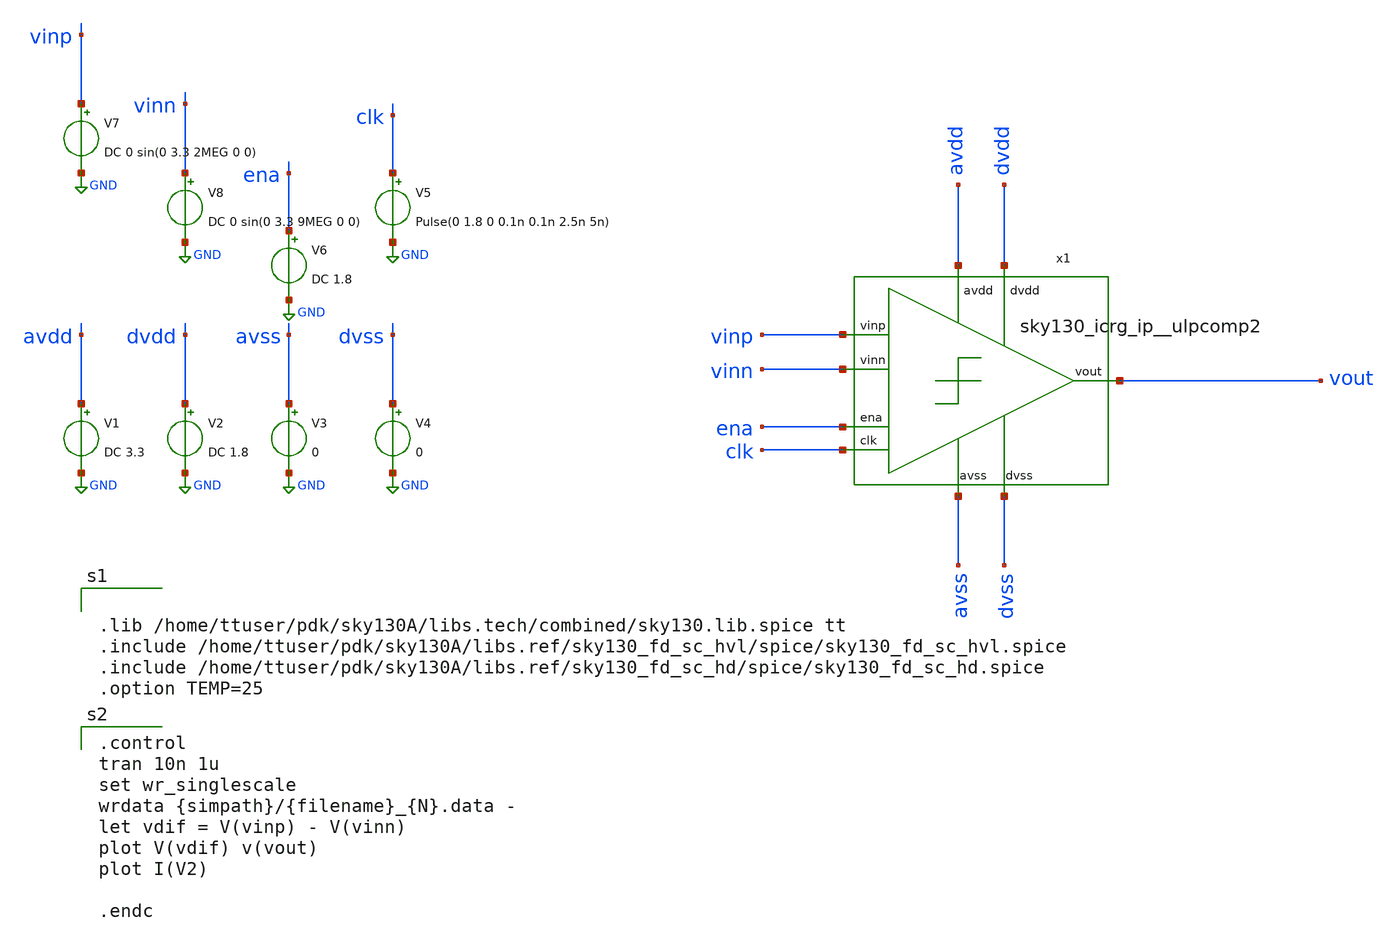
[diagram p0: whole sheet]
** sch_path: xschem/dynamic_current_tb.sch
**.subckt dynamic_current_tb
x1 dvdd avdd ena vout vinn vinp clk dvss avss sky130_icrg_ip__ulpcomp2
V1 avdd GND DC 3.3
V2 dvdd GND DC 1.8
V3 avss GND 0
V4 dvss GND 0
V5 clk GND Pulse(0 1.8 0 0.1n 0.1n 2.5n 5n)
V6 ena GND DC 1.8
V7 vinp GND DC 0 sin(0 3.3 2MEG 0 0)
V8 vinn GND DC 0 sin(0 3.3 9MEG 0 0)
**** begin user architecture code


.lib /home/ttuser/pdk/sky130A/libs.tech/combined/sky130.lib.spice tt
.include /home/ttuser/pdk/sky130A/libs.ref/sky130_fd_sc_hvl/spice/sky130_fd_sc_hvl.spice
.include /home/ttuser/pdk/sky130A/libs.ref/sky130_fd_sc_hd/spice/sky130_fd_sc_hd.spice
.option TEMP=25


.control
tran 10n 1u
set wr_singlescale
wrdata {simpath}/{filename}_{N}.data -
let vdif = V(vinp) - V(vinn)
plot V(vdif) v(vout)
plot I(V2)

.endc

**** end user architecture code
**.ends

* expanding   symbol:  sky130_icrg_ip__ulpcomp2.sym # of pins=9
** sym_path: xschem/sky130_icrg_ip__ulpcomp2.sym
** sch_path: xschem/sky130_icrg_ip__ulpcomp2.sch
.subckt sky130_icrg_ip__ulpcomp2 dvdd avdd ena vout vinn vinp clk dvss avss
*.ipin avdd
*.ipin vinp
*.ipin vinn
*.opin avss
*.opin vout
*.opin dvss
*.ipin dvdd
*.ipin clk
*.ipin ena
x1 dvddb clka clk clkb dvss Stage0_clk_inv
x2 avdd enab clka vinn vinp net2 net1 avss Stage1
x3 dvdd enab dvddb clkb vout net2 net1 dvss Stage2_latch
x4 dvdd ena enab dvss Stage0_ena_inv
.ends


* expanding   symbol:  Stage0_clk_inv.sym # of pins=5
** sym_path: xschem/Stage0_clk_inv.sym
** sch_path: xschem/Stage0_clk_inv.sch
.subckt Stage0_clk_inv dvddb clka clk clkb dvss
*.opin dvss
*.ipin dvddb
*.opin clka
*.ipin clk
*.opin clkb
XM22 clka clkb dvddb dvddb sky130_fd_pr__pfet_01v8 L=0.5 W=2 nf=1 ad='int((nf+1)/2) * W/nf * 0.29' as='int((nf+2)/2) * W/nf * 0.29'
+ pd='2*int((nf+1)/2) * (W/nf + 0.29)' ps='2*int((nf+2)/2) * (W/nf + 0.29)' nrd='0.29 / W' nrs='0.29 / W'
+ sa=0 sb=0 sd=0 mult=1 m=1
XM8 clkb clk dvddb dvddb sky130_fd_pr__pfet_01v8 L=0.5 W=2 nf=1 ad='int((nf+1)/2) * W/nf * 0.29' as='int((nf+2)/2) * W/nf * 0.29'
+ pd='2*int((nf+1)/2) * (W/nf + 0.29)' ps='2*int((nf+2)/2) * (W/nf + 0.29)' nrd='0.29 / W' nrs='0.29 / W'
+ sa=0 sb=0 sd=0 mult=1 m=1
XM6 clkb clk dvss dvss sky130_fd_pr__nfet_01v8 L=0.5 W=1 nf=1 ad='int((nf+1)/2) * W/nf * 0.29' as='int((nf+2)/2) * W/nf * 0.29'
+ pd='2*int((nf+1)/2) * (W/nf + 0.29)' ps='2*int((nf+2)/2) * (W/nf + 0.29)' nrd='0.29 / W' nrs='0.29 / W'
+ sa=0 sb=0 sd=0 mult=1 m=1
XM21 clka clkb dvss dvss sky130_fd_pr__nfet_01v8 L=0.5 W=1 nf=1 ad='int((nf+1)/2) * W/nf * 0.29' as='int((nf+2)/2) * W/nf * 0.29'
+ pd='2*int((nf+1)/2) * (W/nf + 0.29)' ps='2*int((nf+2)/2) * (W/nf + 0.29)' nrd='0.29 / W' nrs='0.29 / W'
+ sa=0 sb=0 sd=0 mult=1 m=1
.ends


* expanding   symbol:  Stage1.sym # of pins=8
** sym_path: xschem/Stage1.sym
** sch_path: xschem/Stage1.sch
.subckt Stage1 avdd enab clka vinn vinp oneg opos avss
*.ipin avdd
*.ipin vinp
*.ipin vinn
*.opin avss
*.opin opos
*.opin oneg
*.ipin clka
*.ipin enab
XM1 net4 net5 avdd avdd sky130_fd_pr__pfet_g5v0d10v5 L=1 W=50 nf=2 ad='int((nf+1)/2) * W/nf * 0.29' as='int((nf+2)/2) * W/nf * 0.29'
+ pd='2*int((nf+1)/2) * (W/nf + 0.29)' ps='2*int((nf+2)/2) * (W/nf + 0.29)' nrd='0.29 / W' nrs='0.29 / W'
+ sa=0 sb=0 sd=0 mult=2 m=2
x2 clka dvdd dvss dvss avdd avdd net2 sky130_fd_sc_hvl__lsbuflv2hv_1
XM6 net1 net2 net4 net4 sky130_fd_pr__pfet_g5v0d10v5 L=1 W=50 nf=2 ad='int((nf+1)/2) * W/nf * 0.29' as='int((nf+2)/2) * W/nf * 0.29'
+ pd='2*int((nf+1)/2) * (W/nf + 0.29)' ps='2*int((nf+2)/2) * (W/nf + 0.29)' nrd='0.29 / W' nrs='0.29 / W'
+ sa=0 sb=0 sd=0 mult=2 m=2
XM2 oneg vinp net1 net1 sky130_fd_pr__pfet_g5v0d10v5 L=1 W=20 nf=2 ad='int((nf+1)/2) * W/nf * 0.29' as='int((nf+2)/2) * W/nf * 0.29'
+ pd='2*int((nf+1)/2) * (W/nf + 0.29)' ps='2*int((nf+2)/2) * (W/nf + 0.29)' nrd='0.29 / W' nrs='0.29 / W'
+ sa=0 sb=0 sd=0 mult=2 m=2
XM3 opos vinn net1 net1 sky130_fd_pr__pfet_g5v0d10v5 L=1 W=20 nf=2 ad='int((nf+1)/2) * W/nf * 0.29' as='int((nf+2)/2) * W/nf * 0.29'
+ pd='2*int((nf+1)/2) * (W/nf + 0.29)' ps='2*int((nf+2)/2) * (W/nf + 0.29)' nrd='0.29 / W' nrs='0.29 / W'
+ sa=0 sb=0 sd=0 mult=2 m=2
XM4 net3 net3 avss avss sky130_fd_pr__nfet_03v3_nvt L=0.5 W=5 nf=1 ad='int((nf+1)/2) * W/nf * 0.29' as='int((nf+2)/2) * W/nf * 0.29'
+ pd='2*int((nf+1)/2) * (W/nf + 0.29)' ps='2*int((nf+2)/2) * (W/nf + 0.29)' nrd='0.29 / W' nrs='0.29 / W'
+ sa=0 sb=0 sd=0 mult=2 m=2
XM8 opos net2 net3 net3 sky130_fd_pr__nfet_g5v0d10v5 L=0.5 W=5 nf=1 ad='int((nf+1)/2) * W/nf * 0.29'
+ as='int((nf+2)/2) * W/nf * 0.29' pd='2*int((nf+1)/2) * (W/nf + 0.29)' ps='2*int((nf+2)/2) * (W/nf + 0.29)'
+ nrd='0.29 / W' nrs='0.29 / W' sa=0 sb=0 sd=0 mult=1 m=1
XM5 oneg net2 net3 net3 sky130_fd_pr__nfet_g5v0d10v5 L=0.5 W=5 nf=1 ad='int((nf+1)/2) * W/nf * 0.29'
+ as='int((nf+2)/2) * W/nf * 0.29' pd='2*int((nf+1)/2) * (W/nf + 0.29)' ps='2*int((nf+2)/2) * (W/nf + 0.29)'
+ nrd='0.29 / W' nrs='0.29 / W' sa=0 sb=0 sd=0 mult=1 m=1
x1 enab dvdd dvss dvss avdd avdd net5 sky130_fd_sc_hvl__lsbuflv2hv_1
.ends


* expanding   symbol:  Stage2_latch.sym # of pins=8
** sym_path: xschem/Stage2_latch.sym
** sch_path: xschem/Stage2_latch.sch
.subckt Stage2_latch dvdd enab dvddb clkb vout oneg opos dvss
*.ipin clkb
*.opin vout
*.opin dvss
*.ipin dvdd
*.ipin opos
*.ipin oneg
*.ipin enab
*.opin dvddb
XM18 vout net1 dvss dvss sky130_fd_pr__nfet_01v8 L=0.5 W=1 nf=1 ad='int((nf+1)/2) * W/nf * 0.29' as='int((nf+2)/2) * W/nf * 0.29'
+ pd='2*int((nf+1)/2) * (W/nf + 0.29)' ps='2*int((nf+2)/2) * (W/nf + 0.29)' nrd='0.29 / W' nrs='0.29 / W'
+ sa=0 sb=0 sd=0 mult=1 m=1
XM19 vout net1 dvddb dvddb sky130_fd_pr__pfet_01v8 L=1 W=2 nf=1 ad='int((nf+1)/2) * W/nf * 0.29' as='int((nf+2)/2) * W/nf * 0.29'
+ pd='2*int((nf+1)/2) * (W/nf + 0.29)' ps='2*int((nf+2)/2) * (W/nf + 0.29)' nrd='0.29 / W' nrs='0.29 / W'
+ sa=0 sb=0 sd=0 mult=1 m=1
XM15 net5 clkb dvss dvss sky130_fd_pr__nfet_03v3_nvt L=0.5 W=2 nf=1 ad='int((nf+1)/2) * W/nf * 0.29'
+ as='int((nf+2)/2) * W/nf * 0.29' pd='2*int((nf+1)/2) * (W/nf + 0.29)' ps='2*int((nf+2)/2) * (W/nf + 0.29)'
+ nrd='0.29 / W' nrs='0.29 / W' sa=0 sb=0 sd=0 mult=1 m=1
XM9 net1 clkb dvddb dvddb sky130_fd_pr__pfet_01v8_hvt L=1 W=3 nf=1 ad='int((nf+1)/2) * W/nf * 0.29' as='int((nf+2)/2) * W/nf * 0.29'
+ pd='2*int((nf+1)/2) * (W/nf + 0.29)' ps='2*int((nf+2)/2) * (W/nf + 0.29)' nrd='0.29 / W' nrs='0.29 / W'
+ sa=0 sb=0 sd=0 mult=2 m=2
XM10 net2 net1 dvddb dvddb sky130_fd_pr__pfet_01v8_hvt L=1 W=3 nf=1 ad='int((nf+1)/2) * W/nf * 0.29'
+ as='int((nf+2)/2) * W/nf * 0.29' pd='2*int((nf+1)/2) * (W/nf + 0.29)' ps='2*int((nf+2)/2) * (W/nf + 0.29)'
+ nrd='0.29 / W' nrs='0.29 / W' sa=0 sb=0 sd=0 mult=2 m=2
XM11 net1 net2 dvddb dvddb sky130_fd_pr__pfet_01v8_hvt L=1 W=3 nf=1 ad='int((nf+1)/2) * W/nf * 0.29'
+ as='int((nf+2)/2) * W/nf * 0.29' pd='2*int((nf+1)/2) * (W/nf + 0.29)' ps='2*int((nf+2)/2) * (W/nf + 0.29)'
+ nrd='0.29 / W' nrs='0.29 / W' sa=0 sb=0 sd=0 mult=2 m=2
XM12 net2 clkb dvddb dvddb sky130_fd_pr__pfet_01v8_hvt L=1 W=3 nf=1 ad='int((nf+1)/2) * W/nf * 0.29'
+ as='int((nf+2)/2) * W/nf * 0.29' pd='2*int((nf+1)/2) * (W/nf + 0.29)' ps='2*int((nf+2)/2) * (W/nf + 0.29)'
+ nrd='0.29 / W' nrs='0.29 / W' sa=0 sb=0 sd=0 mult=2 m=2
XM1 dvddb enab dvdd dvdd sky130_fd_pr__pfet_01v8_hvt L=1 W=3 nf=1 ad='int((nf+1)/2) * W/nf * 0.29' as='int((nf+2)/2) * W/nf * 0.29'
+ pd='2*int((nf+1)/2) * (W/nf + 0.29)' ps='2*int((nf+2)/2) * (W/nf + 0.29)' nrd='0.29 / W' nrs='0.29 / W'
+ sa=0 sb=0 sd=0 mult=2 m=2
XM2 net1 opos net3 dvss sky130_fd_pr__nfet_03v3_nvt L=0.5 W=1 nf=1 ad='int((nf+1)/2) * W/nf * 0.29' as='int((nf+2)/2) * W/nf * 0.29'
+ pd='2*int((nf+1)/2) * (W/nf + 0.29)' ps='2*int((nf+2)/2) * (W/nf + 0.29)' nrd='0.29 / W' nrs='0.29 / W'
+ sa=0 sb=0 sd=0 mult=1 m=1
XM3 net4 net1 net5 dvss sky130_fd_pr__nfet_03v3_nvt L=0.5 W=1 nf=1 ad='int((nf+1)/2) * W/nf * 0.29' as='int((nf+2)/2) * W/nf * 0.29'
+ pd='2*int((nf+1)/2) * (W/nf + 0.29)' ps='2*int((nf+2)/2) * (W/nf + 0.29)' nrd='0.29 / W' nrs='0.29 / W'
+ sa=0 sb=0 sd=0 mult=1 m=1
XM4 net3 net2 net5 dvss sky130_fd_pr__nfet_03v3_nvt L=0.5 W=1 nf=1 ad='int((nf+1)/2) * W/nf * 0.29' as='int((nf+2)/2) * W/nf * 0.29'
+ pd='2*int((nf+1)/2) * (W/nf + 0.29)' ps='2*int((nf+2)/2) * (W/nf + 0.29)' nrd='0.29 / W' nrs='0.29 / W'
+ sa=0 sb=0 sd=0 mult=1 m=1
XM5 net2 oneg net4 dvss sky130_fd_pr__nfet_03v3_nvt L=0.5 W=1 nf=1 ad='int((nf+1)/2) * W/nf * 0.29' as='int((nf+2)/2) * W/nf * 0.29'
+ pd='2*int((nf+1)/2) * (W/nf + 0.29)' ps='2*int((nf+2)/2) * (W/nf + 0.29)' nrd='0.29 / W' nrs='0.29 / W'
+ sa=0 sb=0 sd=0 mult=1 m=1
.ends


* expanding   symbol:  Stage0_ena_inv.sym # of pins=4
** sym_path: xschem/Stage0_ena_inv.sym
** sch_path: xschem/Stage0_ena_inv.sch
.subckt Stage0_ena_inv dvdd ena enab dvss
*.ipin ena
*.ipin dvdd
*.ipin dvss
*.opin enab
XM25 enab ena dvdd dvdd sky130_fd_pr__pfet_01v8 L=0.5 W=2 nf=1 ad='int((nf+1)/2) * W/nf * 0.29' as='int((nf+2)/2) * W/nf * 0.29'
+ pd='2*int((nf+1)/2) * (W/nf + 0.29)' ps='2*int((nf+2)/2) * (W/nf + 0.29)' nrd='0.29 / W' nrs='0.29 / W'
+ sa=0 sb=0 sd=0 mult=1 m=1
XM24 enab ena dvss dvss sky130_fd_pr__nfet_01v8 L=0.5 W=1 nf=1 ad='int((nf+1)/2) * W/nf * 0.29' as='int((nf+2)/2) * W/nf * 0.29'
+ pd='2*int((nf+1)/2) * (W/nf + 0.29)' ps='2*int((nf+2)/2) * (W/nf + 0.29)' nrd='0.29 / W' nrs='0.29 / W'
+ sa=0 sb=0 sd=0 mult=1 m=1
.ends

.GLOBAL GND
.end
